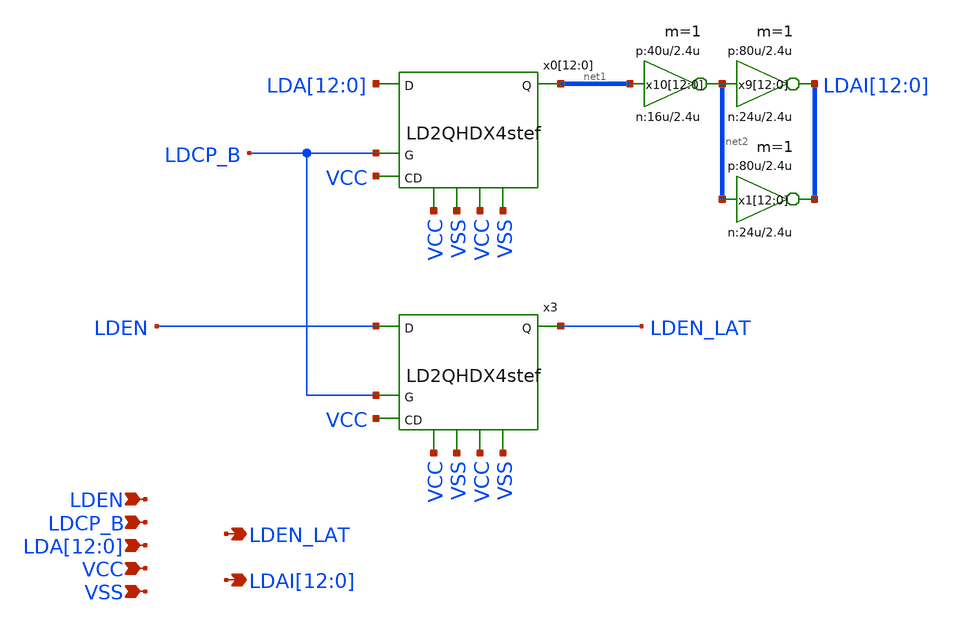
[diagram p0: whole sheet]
** sch_path: xschem_libs_newsym/rom8k/rom2_addlatch/schematic/rom2_addlatch.sch
* Copyright (C) 1998-2024 Stefan Frederik Schippers
* This program is free software; you can redistribute it and/or modify
* it under the terms of the GNU General Public License as published by
* the Free Software Foundation; either version 2 of the License, or
* (at your option) any later version.
* This program is distributed in the hope that it will be useful,
* but WITHOUT ANY WARRANTY; without even the implied warranty of
* MERCHANTABILITY or FITNESS FOR A PARTICULAR PURPOSE.  See the
* GNU General Public License for more details.
* You should have received a copy of the GNU General Public License
* along with this program; if not, write to the Free Software
**.subckt rom2_addlatch LDEN_LAT
*+ LDAI[12],LDAI[11],LDAI[10],LDAI[9],LDAI[8],LDAI[7],LDAI[6],LDAI[5],LDAI[4],LDAI[3],LDAI[2],LDAI[1],LDAI[0] LDEN LDCP_B
*+ LDA[12],LDA[11],LDA[10],LDA[9],LDA[8],LDA[7],LDA[6],LDA[5],LDA[4],LDA[3],LDA[2],LDA[1],LDA[0] VCC VSS
*.opin LDEN_LAT
*.opin
*+ LDAI[12],LDAI[11],LDAI[10],LDAI[9],LDAI[8],LDAI[7],LDAI[6],LDAI[5],LDAI[4],LDAI[3],LDAI[2],LDAI[1],LDAI[0]
*.ipin LDEN
*.ipin LDCP_B
*.ipin LDA[12],LDA[11],LDA[10],LDA[9],LDA[8],LDA[7],LDA[6],LDA[5],LDA[4],LDA[3],LDA[2],LDA[1],LDA[0]
*.ipin VCC
*.ipin VSS
x0[12] LDA[12] LDCP_B VCC net1[12] VCC VSS VCC VSS LD2QHDX4stef
x0[11] LDA[11] LDCP_B VCC net1[11] VCC VSS VCC VSS LD2QHDX4stef
x0[10] LDA[10] LDCP_B VCC net1[10] VCC VSS VCC VSS LD2QHDX4stef
x0[9] LDA[9] LDCP_B VCC net1[9] VCC VSS VCC VSS LD2QHDX4stef
x0[8] LDA[8] LDCP_B VCC net1[8] VCC VSS VCC VSS LD2QHDX4stef
x0[7] LDA[7] LDCP_B VCC net1[7] VCC VSS VCC VSS LD2QHDX4stef
x0[6] LDA[6] LDCP_B VCC net1[6] VCC VSS VCC VSS LD2QHDX4stef
x0[5] LDA[5] LDCP_B VCC net1[5] VCC VSS VCC VSS LD2QHDX4stef
x0[4] LDA[4] LDCP_B VCC net1[4] VCC VSS VCC VSS LD2QHDX4stef
x0[3] LDA[3] LDCP_B VCC net1[3] VCC VSS VCC VSS LD2QHDX4stef
x0[2] LDA[2] LDCP_B VCC net1[2] VCC VSS VCC VSS LD2QHDX4stef
x0[1] LDA[1] LDCP_B VCC net1[1] VCC VSS VCC VSS LD2QHDX4stef
x0[0] LDA[0] LDCP_B VCC net1[0] VCC VSS VCC VSS LD2QHDX4stef
x9[12] LDAI[12] net2[12] vcc vss lvnot wn=24u lln=2.4u wp=80u lp=2.4u m=1
x9[11] LDAI[11] net2[11] vcc vss lvnot wn=24u lln=2.4u wp=80u lp=2.4u m=1
x9[10] LDAI[10] net2[10] vcc vss lvnot wn=24u lln=2.4u wp=80u lp=2.4u m=1
x9[9] LDAI[9] net2[9] vcc vss lvnot wn=24u lln=2.4u wp=80u lp=2.4u m=1
x9[8] LDAI[8] net2[8] vcc vss lvnot wn=24u lln=2.4u wp=80u lp=2.4u m=1
x9[7] LDAI[7] net2[7] vcc vss lvnot wn=24u lln=2.4u wp=80u lp=2.4u m=1
x9[6] LDAI[6] net2[6] vcc vss lvnot wn=24u lln=2.4u wp=80u lp=2.4u m=1
x9[5] LDAI[5] net2[5] vcc vss lvnot wn=24u lln=2.4u wp=80u lp=2.4u m=1
x9[4] LDAI[4] net2[4] vcc vss lvnot wn=24u lln=2.4u wp=80u lp=2.4u m=1
x9[3] LDAI[3] net2[3] vcc vss lvnot wn=24u lln=2.4u wp=80u lp=2.4u m=1
x9[2] LDAI[2] net2[2] vcc vss lvnot wn=24u lln=2.4u wp=80u lp=2.4u m=1
x9[1] LDAI[1] net2[1] vcc vss lvnot wn=24u lln=2.4u wp=80u lp=2.4u m=1
x9[0] LDAI[0] net2[0] vcc vss lvnot wn=24u lln=2.4u wp=80u lp=2.4u m=1
x10[12] net2[12] net1[12] vcc vss lvnot wn=16u lln=2.4u wp=40u lp=2.4u m=1
x10[11] net2[11] net1[11] vcc vss lvnot wn=16u lln=2.4u wp=40u lp=2.4u m=1
x10[10] net2[10] net1[10] vcc vss lvnot wn=16u lln=2.4u wp=40u lp=2.4u m=1
x10[9] net2[9] net1[9] vcc vss lvnot wn=16u lln=2.4u wp=40u lp=2.4u m=1
x10[8] net2[8] net1[8] vcc vss lvnot wn=16u lln=2.4u wp=40u lp=2.4u m=1
x10[7] net2[7] net1[7] vcc vss lvnot wn=16u lln=2.4u wp=40u lp=2.4u m=1
x10[6] net2[6] net1[6] vcc vss lvnot wn=16u lln=2.4u wp=40u lp=2.4u m=1
x10[5] net2[5] net1[5] vcc vss lvnot wn=16u lln=2.4u wp=40u lp=2.4u m=1
x10[4] net2[4] net1[4] vcc vss lvnot wn=16u lln=2.4u wp=40u lp=2.4u m=1
x10[3] net2[3] net1[3] vcc vss lvnot wn=16u lln=2.4u wp=40u lp=2.4u m=1
x10[2] net2[2] net1[2] vcc vss lvnot wn=16u lln=2.4u wp=40u lp=2.4u m=1
x10[1] net2[1] net1[1] vcc vss lvnot wn=16u lln=2.4u wp=40u lp=2.4u m=1
x10[0] net2[0] net1[0] vcc vss lvnot wn=16u lln=2.4u wp=40u lp=2.4u m=1
x3 LDEN LDCP_B VCC LDEN_LAT VCC VSS VCC VSS LD2QHDX4stef
x1[12] LDAI[12] net2[12] vcc vss lvnot wn=24u lln=2.4u wp=80u lp=2.4u m=1
x1[11] LDAI[11] net2[11] vcc vss lvnot wn=24u lln=2.4u wp=80u lp=2.4u m=1
x1[10] LDAI[10] net2[10] vcc vss lvnot wn=24u lln=2.4u wp=80u lp=2.4u m=1
x1[9] LDAI[9] net2[9] vcc vss lvnot wn=24u lln=2.4u wp=80u lp=2.4u m=1
x1[8] LDAI[8] net2[8] vcc vss lvnot wn=24u lln=2.4u wp=80u lp=2.4u m=1
x1[7] LDAI[7] net2[7] vcc vss lvnot wn=24u lln=2.4u wp=80u lp=2.4u m=1
x1[6] LDAI[6] net2[6] vcc vss lvnot wn=24u lln=2.4u wp=80u lp=2.4u m=1
x1[5] LDAI[5] net2[5] vcc vss lvnot wn=24u lln=2.4u wp=80u lp=2.4u m=1
x1[4] LDAI[4] net2[4] vcc vss lvnot wn=24u lln=2.4u wp=80u lp=2.4u m=1
x1[3] LDAI[3] net2[3] vcc vss lvnot wn=24u lln=2.4u wp=80u lp=2.4u m=1
x1[2] LDAI[2] net2[2] vcc vss lvnot wn=24u lln=2.4u wp=80u lp=2.4u m=1
x1[1] LDAI[1] net2[1] vcc vss lvnot wn=24u lln=2.4u wp=80u lp=2.4u m=1
x1[0] LDAI[0] net2[0] vcc vss lvnot wn=24u lln=2.4u wp=80u lp=2.4u m=1
**.ends
.end
